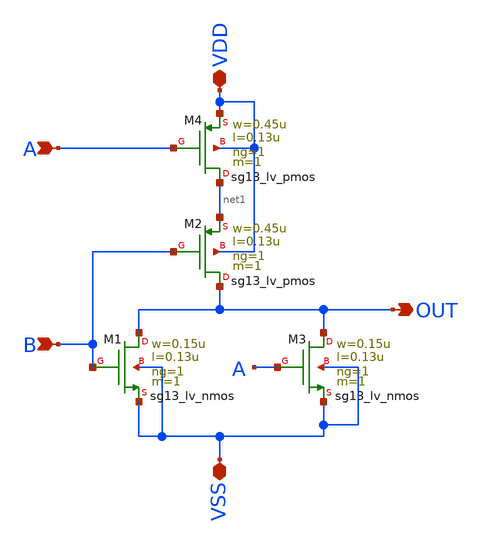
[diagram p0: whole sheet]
** sch_path: Custom_std_cells/nor_custom.sch
**.subckt nor_custom VDD VSS A B OUT
*.iopin VDD
*.iopin VSS
*.ipin A
*.ipin B
*.opin OUT
XM1 OUT B VSS VSS sg13_lv_nmos w=0.15u l=0.13u ng=1 m=1 mm_ok=1
XM2 OUT B net1 VDD sg13_lv_pmos w=0.45u l=0.13u ng=1 m=1 mm_ok=1
XM3 OUT A VSS VSS sg13_lv_nmos w=0.15u l=0.13u ng=1 m=1 mm_ok=1
XM4 net1 A VDD VDD sg13_lv_pmos w=0.45u l=0.13u ng=1 m=1 mm_ok=1
**.ends
.end
